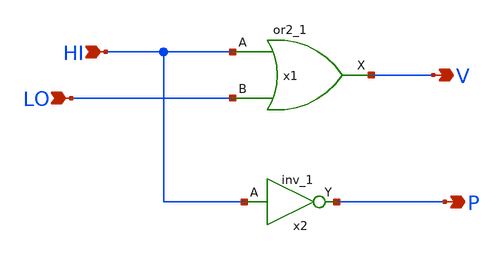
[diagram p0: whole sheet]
** sch_path: frontend/xschem/lzc2.sch
**.subckt lzc2 HI LO V P
*.ipin HI
*.ipin LO
*.opin V
*.opin P
x1 HI LO VGND VNB VPB VPWR V sky130_fd_sc_hd__or2_1
x2 HI GND GND VDD VDD P sky130_fd_sc_hd__inv_1
**.ends
.end
